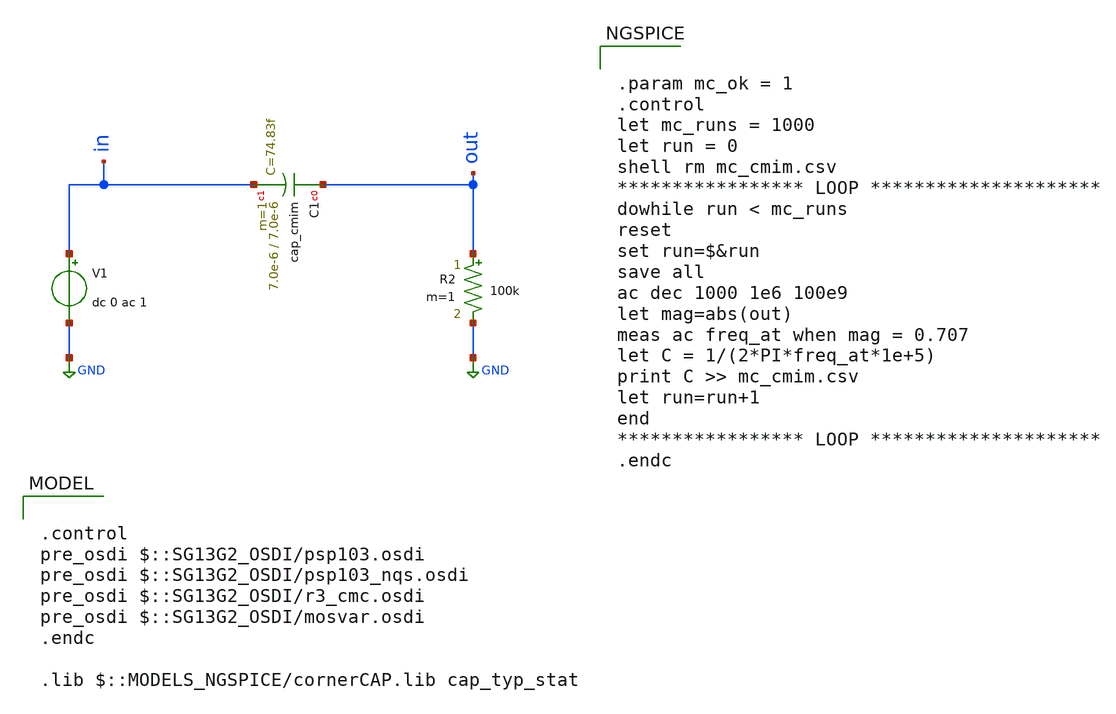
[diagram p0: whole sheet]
** sch_path: ihp-sg13g2/xschem_libs/sg13g2_tests/mc_mim_cap_ac/schematic/mc_mim_cap_ac.sch
* Copyright 2021 Stefan Frederik Schippers
* Licensed under the Apache License, Version 2.0 (the "License");
* you may not use this file except in compliance with the License.
* You may obtain a copy of the License at
* https://www.apache.org/licenses/LICENSE-2.0
* Unless required by applicable law or agreed to in writing, software
* distributed under the License is distributed on an "AS IS" BASIS,
* WITHOUT WARRANTIES OR CONDITIONS OF ANY KIND, either express or implied.
* See the License for the specific language governing permissions and
* limitations under the License.
* Copyright 2023 IHP PDK Authors
**.subckt mc_mim_cap_ac
V1 in GND dc 0 ac 1
R2 out GND 100k m=1
XC1 out in cap_cmim w=7.0e-6 l=7.0e-6 m=1 mm_ok=1
**** begin user architecture code


.param mc_ok = 1
.control
let mc_runs = 1000
let run = 0
shell rm mc_cmim.csv
***************** LOOP *********************
dowhile run < mc_runs
reset
set run=$&run
save all
ac dec 1000 1e6 100e9
let mag=abs(out)
meas ac freq_at when mag = 0.707
let C = 1/(2*PI*freq_at*1e+5)
print C >> mc_cmim.csv
let run=run+1
end
***************** LOOP *********************
.endc



.control
pre_osdi $::SG13G2_OSDI/psp103.osdi
pre_osdi $::SG13G2_OSDI/psp103_nqs.osdi
pre_osdi $::SG13G2_OSDI/r3_cmc.osdi
pre_osdi $::SG13G2_OSDI/mosvar.osdi
.endc

.lib $::MODELS_NGSPICE/cornerCAP.lib cap_typ_stat

**** end user architecture code
**.ends
.GLOBAL GND
.end
